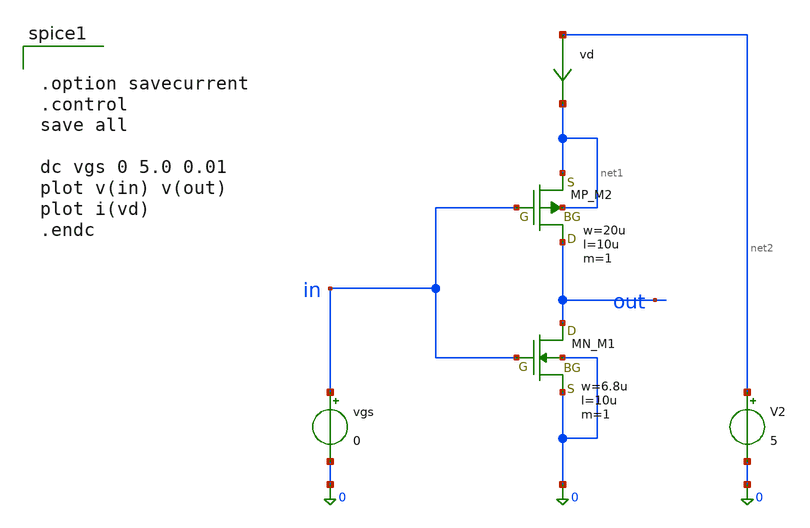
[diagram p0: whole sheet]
** sch_path: member_project/JJY_Receiver/Masahiro/jjy_recv/pre_amp/inverter_sim.sch
**.subckt inverter_sim
XM1 out in 0 0 NMOS w=6.8u l=10u as=0 ad=0 ps=0 pd=0 nrd=0 nrs=0 m=1
XM2 out in net1 net1 PMOS w=20u l=10u as=0 ad=0 ps=0 pd=0 nrd=0 nrs=0 m=1
vgs in 0 0
V2 net2 0 5
vd net2 net1 0
.save i(vd)
**** begin user architecture code
 .include $::LIB/ip62_models


.option savecurrent
.control
save all

dc vgs 0 5.0 0.01
plot v(in) v(out)
plot i(vd)
.endc


**** end user architecture code
**.ends
.end
